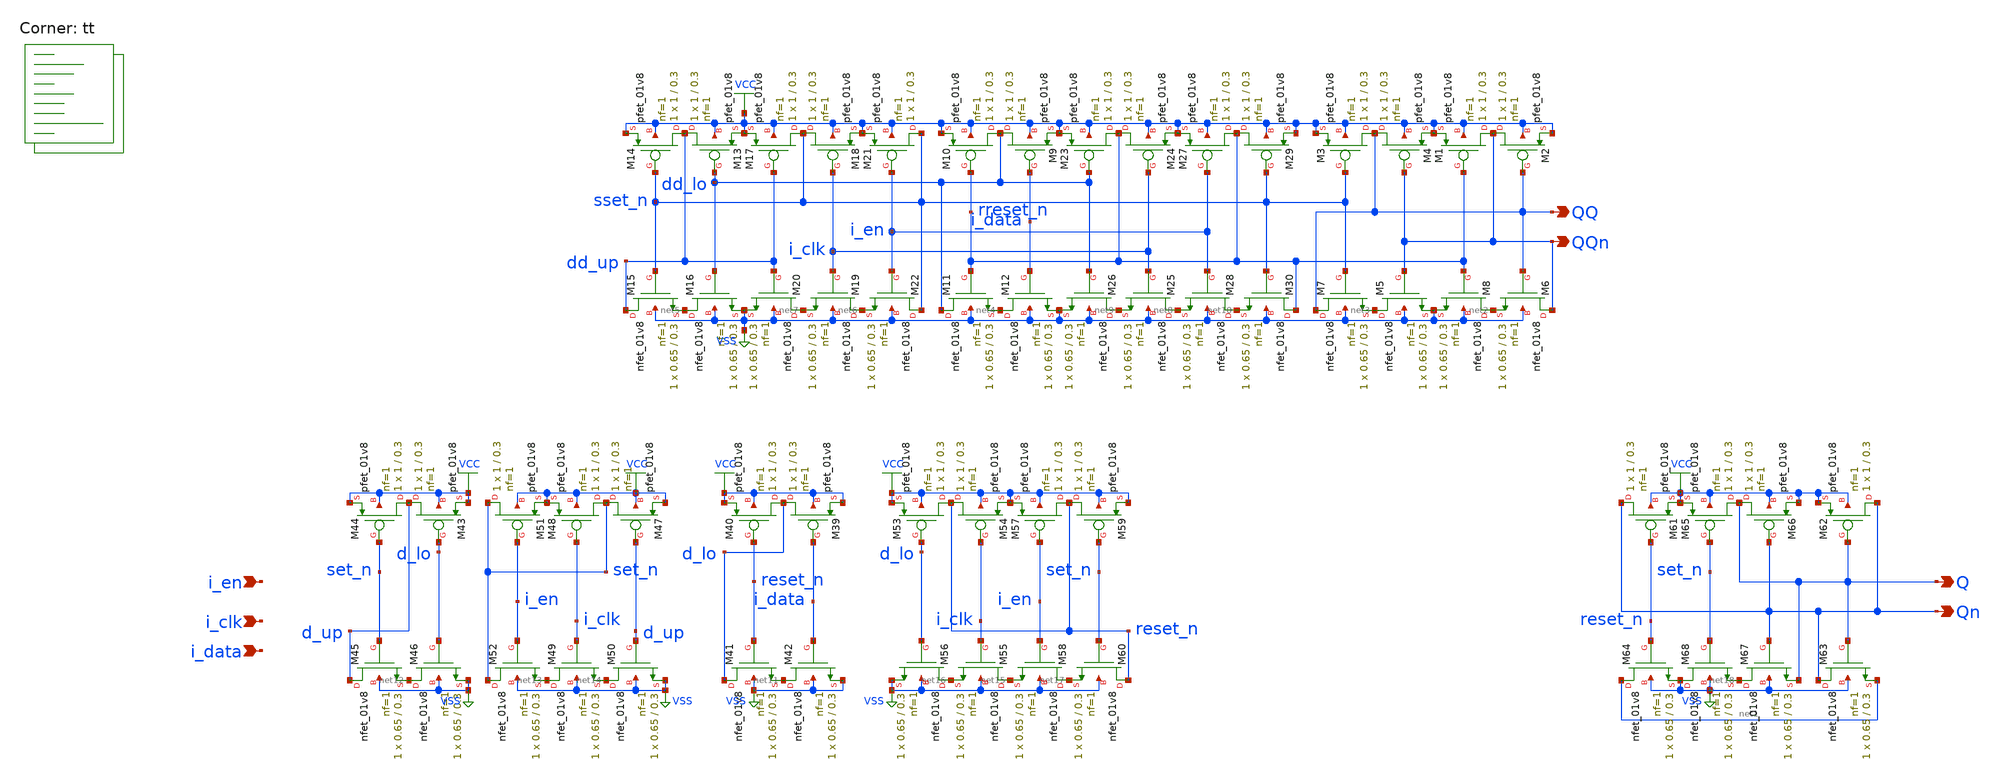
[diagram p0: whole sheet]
** sch_path: elements/edffe.sch
**.subckt edffe QQ QQn i_clk i_data i_en Q Qn
*.opin QQ
*.opin QQn
*.ipin i_clk
*.ipin i_data
*.ipin i_en
*.opin Q
*.opin Qn
XM1 QQn rreset_n VCC VCC sky130_fd_pr__pfet_01v8 L=0.3 W=1 nf=1 ad='int((nf+1)/2) * W/nf * 0.29' as='int((nf+2)/2) * W/nf * 0.29'
+ pd='2*int((nf+1)/2) * (W/nf + 0.29)' ps='2*int((nf+2)/2) * (W/nf + 0.29)' nrd='0.29 / W' nrs='0.29 / W'
+ sa=0 sb=0 sd=0 mult=1 m=1
XM2 QQn QQ VCC VCC sky130_fd_pr__pfet_01v8 L=0.3 W=1 nf=1 ad='int((nf+1)/2) * W/nf * 0.29' as='int((nf+2)/2) * W/nf * 0.29'
+ pd='2*int((nf+1)/2) * (W/nf + 0.29)' ps='2*int((nf+2)/2) * (W/nf + 0.29)' nrd='0.29 / W' nrs='0.29 / W'
+ sa=0 sb=0 sd=0 mult=1 m=1
XM6 QQn QQ net2 VSS sky130_fd_pr__nfet_01v8 L=0.3 W=0.65 nf=1 ad='int((1 + 1)/2) * 0.65 / 1 * 0.29' as='int((1 + 2)/2) * 0.65 / 1 * 0.29'
+ pd='2*int((1 + 1)/2) * (0.65 / 1 + 0.29)' ps='2*int((1 + 2)/2) * (0.65 / 1 + 0.29)' nrd='0.29 / 0.65 '
+ nrs='0.29 / 0.65 ' sa=0 sb=0 sd=0 mult=1 m=1
XM8 net2 rreset_n VSS VSS sky130_fd_pr__nfet_01v8 L=0.3 W=0.65 nf=1 ad='int((1 + 1)/2) * 0.65 / 1 * 0.29'
+ as='int((1 + 2)/2) * 0.65 / 1 * 0.29' pd='2*int((1 + 1)/2) * (0.65 / 1 + 0.29)' ps='2*int((1 + 2)/2) * (0.65 / 1 + 0.29)'
+ nrd='0.29 / 0.65 ' nrs='0.29 / 0.65 ' sa=0 sb=0 sd=0 mult=1 m=1
XM3 QQ sset_n VCC VCC sky130_fd_pr__pfet_01v8 L=0.3 W=1 nf=1 ad='int((nf+1)/2) * W/nf * 0.29' as='int((nf+2)/2) * W/nf * 0.29'
+ pd='2*int((nf+1)/2) * (W/nf + 0.29)' ps='2*int((nf+2)/2) * (W/nf + 0.29)' nrd='0.29 / W' nrs='0.29 / W'
+ sa=0 sb=0 sd=0 mult=1 m=1
XM4 QQ QQn VCC VCC sky130_fd_pr__pfet_01v8 L=0.3 W=1 nf=1 ad='int((nf+1)/2) * W/nf * 0.29' as='int((nf+2)/2) * W/nf * 0.29'
+ pd='2*int((nf+1)/2) * (W/nf + 0.29)' ps='2*int((nf+2)/2) * (W/nf + 0.29)' nrd='0.29 / W' nrs='0.29 / W'
+ sa=0 sb=0 sd=0 mult=1 m=1
XM5 net3 QQn VSS VSS sky130_fd_pr__nfet_01v8 L=0.3 W=0.65 nf=1 ad='int((1 + 1)/2) * 0.65 / 1 * 0.29'
+ as='int((1 + 2)/2) * 0.65 / 1 * 0.29' pd='2*int((1 + 1)/2) * (0.65 / 1 + 0.29)' ps='2*int((1 + 2)/2) * (0.65 / 1 + 0.29)'
+ nrd='0.29 / 0.65 ' nrs='0.29 / 0.65 ' sa=0 sb=0 sd=0 mult=1 m=1
XM7 QQ sset_n net3 VSS sky130_fd_pr__nfet_01v8 L=0.3 W=0.65 nf=1 ad='int((1 + 1)/2) * 0.65 / 1 * 0.29'
+ as='int((1 + 2)/2) * 0.65 / 1 * 0.29' pd='2*int((1 + 1)/2) * (0.65 / 1 + 0.29)' ps='2*int((1 + 2)/2) * (0.65 / 1 + 0.29)'
+ nrd='0.29 / 0.65 ' nrs='0.29 / 0.65 ' sa=0 sb=0 sd=0 mult=1 m=1
XM9 dd_lo i_data VCC VCC sky130_fd_pr__pfet_01v8 L=0.3 W=1 nf=1 ad='int((nf+1)/2) * W/nf * 0.29' as='int((nf+2)/2) * W/nf * 0.29'
+ pd='2*int((nf+1)/2) * (W/nf + 0.29)' ps='2*int((nf+2)/2) * (W/nf + 0.29)' nrd='0.29 / W' nrs='0.29 / W'
+ sa=0 sb=0 sd=0 mult=1 m=1
XM10 dd_lo rreset_n VCC VCC sky130_fd_pr__pfet_01v8 L=0.3 W=1 nf=1 ad='int((nf+1)/2) * W/nf * 0.29' as='int((nf+2)/2) * W/nf * 0.29'
+ pd='2*int((nf+1)/2) * (W/nf + 0.29)' ps='2*int((nf+2)/2) * (W/nf + 0.29)' nrd='0.29 / W' nrs='0.29 / W'
+ sa=0 sb=0 sd=0 mult=1 m=1
XM11 dd_lo rreset_n net4 VSS sky130_fd_pr__nfet_01v8 L=0.3 W=0.65 nf=1 ad='int((1 + 1)/2) * 0.65 / 1 * 0.29'
+ as='int((1 + 2)/2) * 0.65 / 1 * 0.29' pd='2*int((1 + 1)/2) * (0.65 / 1 + 0.29)' ps='2*int((1 + 2)/2) * (0.65 / 1 + 0.29)'
+ nrd='0.29 / 0.65 ' nrs='0.29 / 0.65 ' sa=0 sb=0 sd=0 mult=1 m=1
XM12 net4 i_data VSS VSS sky130_fd_pr__nfet_01v8 L=0.3 W=0.65 nf=1 ad='int((1 + 1)/2) * 0.65 / 1 * 0.29'
+ as='int((1 + 2)/2) * 0.65 / 1 * 0.29' pd='2*int((1 + 1)/2) * (0.65 / 1 + 0.29)' ps='2*int((1 + 2)/2) * (0.65 / 1 + 0.29)'
+ nrd='0.29 / 0.65 ' nrs='0.29 / 0.65 ' sa=0 sb=0 sd=0 mult=1 m=1
XM13 dd_up dd_lo VCC VCC sky130_fd_pr__pfet_01v8 L=0.3 W=1 nf=1 ad='int((nf+1)/2) * W/nf * 0.29' as='int((nf+2)/2) * W/nf * 0.29'
+ pd='2*int((nf+1)/2) * (W/nf + 0.29)' ps='2*int((nf+2)/2) * (W/nf + 0.29)' nrd='0.29 / W' nrs='0.29 / W'
+ sa=0 sb=0 sd=0 mult=1 m=1
XM14 dd_up sset_n VCC VCC sky130_fd_pr__pfet_01v8 L=0.3 W=1 nf=1 ad='int((nf+1)/2) * W/nf * 0.29' as='int((nf+2)/2) * W/nf * 0.29'
+ pd='2*int((nf+1)/2) * (W/nf + 0.29)' ps='2*int((nf+2)/2) * (W/nf + 0.29)' nrd='0.29 / W' nrs='0.29 / W'
+ sa=0 sb=0 sd=0 mult=1 m=1
XM15 dd_up sset_n net5 VSS sky130_fd_pr__nfet_01v8 L=0.3 W=0.65 nf=1 ad='int((1 + 1)/2) * 0.65 / 1 * 0.29'
+ as='int((1 + 2)/2) * 0.65 / 1 * 0.29' pd='2*int((1 + 1)/2) * (0.65 / 1 + 0.29)' ps='2*int((1 + 2)/2) * (0.65 / 1 + 0.29)'
+ nrd='0.29 / 0.65 ' nrs='0.29 / 0.65 ' sa=0 sb=0 sd=0 mult=1 m=1
XM16 net5 dd_lo VSS VSS sky130_fd_pr__nfet_01v8 L=0.3 W=0.65 nf=1 ad='int((1 + 1)/2) * 0.65 / 1 * 0.29'
+ as='int((1 + 2)/2) * 0.65 / 1 * 0.29' pd='2*int((1 + 1)/2) * (0.65 / 1 + 0.29)' ps='2*int((1 + 2)/2) * (0.65 / 1 + 0.29)'
+ nrd='0.29 / 0.65 ' nrs='0.29 / 0.65 ' sa=0 sb=0 sd=0 mult=1 m=1
XM17 sset_n dd_up VCC VCC sky130_fd_pr__pfet_01v8 L=0.3 W=1 nf=1 ad='int((nf+1)/2) * W/nf * 0.29' as='int((nf+2)/2) * W/nf * 0.29'
+ pd='2*int((nf+1)/2) * (W/nf + 0.29)' ps='2*int((nf+2)/2) * (W/nf + 0.29)' nrd='0.29 / W' nrs='0.29 / W'
+ sa=0 sb=0 sd=0 mult=1 m=1
XM18 sset_n i_clk VCC VCC sky130_fd_pr__pfet_01v8 L=0.3 W=1 nf=1 ad='int((nf+1)/2) * W/nf * 0.29' as='int((nf+2)/2) * W/nf * 0.29'
+ pd='2*int((nf+1)/2) * (W/nf + 0.29)' ps='2*int((nf+2)/2) * (W/nf + 0.29)' nrd='0.29 / W' nrs='0.29 / W'
+ sa=0 sb=0 sd=0 mult=1 m=1
XM19 net6 i_clk net7 VSS sky130_fd_pr__nfet_01v8 L=0.3 W=0.65 nf=1 ad='int((1 + 1)/2) * 0.65 / 1 * 0.29'
+ as='int((1 + 2)/2) * 0.65 / 1 * 0.29' pd='2*int((1 + 1)/2) * (0.65 / 1 + 0.29)' ps='2*int((1 + 2)/2) * (0.65 / 1 + 0.29)'
+ nrd='0.29 / 0.65 ' nrs='0.29 / 0.65 ' sa=0 sb=0 sd=0 mult=1 m=1
XM20 net7 dd_up VSS VSS sky130_fd_pr__nfet_01v8 L=0.3 W=0.65 nf=1 ad='int((1 + 1)/2) * 0.65 / 1 * 0.29'
+ as='int((1 + 2)/2) * 0.65 / 1 * 0.29' pd='2*int((1 + 1)/2) * (0.65 / 1 + 0.29)' ps='2*int((1 + 2)/2) * (0.65 / 1 + 0.29)'
+ nrd='0.29 / 0.65 ' nrs='0.29 / 0.65 ' sa=0 sb=0 sd=0 mult=1 m=1
XM21 sset_n i_en VCC VCC sky130_fd_pr__pfet_01v8 L=0.3 W=1 nf=1 ad='int((nf+1)/2) * W/nf * 0.29' as='int((nf+2)/2) * W/nf * 0.29'
+ pd='2*int((nf+1)/2) * (W/nf + 0.29)' ps='2*int((nf+2)/2) * (W/nf + 0.29)' nrd='0.29 / W' nrs='0.29 / W'
+ sa=0 sb=0 sd=0 mult=1 m=1
XM22 sset_n i_en net6 VSS sky130_fd_pr__nfet_01v8 L=0.3 W=0.65 nf=1 ad='int((1 + 1)/2) * 0.65 / 1 * 0.29'
+ as='int((1 + 2)/2) * 0.65 / 1 * 0.29' pd='2*int((1 + 1)/2) * (0.65 / 1 + 0.29)' ps='2*int((1 + 2)/2) * (0.65 / 1 + 0.29)'
+ nrd='0.29 / 0.65 ' nrs='0.29 / 0.65 ' sa=0 sb=0 sd=0 mult=1 m=1
XM23 rreset_n dd_lo VCC VCC sky130_fd_pr__pfet_01v8 L=0.3 W=1 nf=1 ad='int((nf+1)/2) * W/nf * 0.29' as='int((nf+2)/2) * W/nf * 0.29'
+ pd='2*int((nf+1)/2) * (W/nf + 0.29)' ps='2*int((nf+2)/2) * (W/nf + 0.29)' nrd='0.29 / W' nrs='0.29 / W'
+ sa=0 sb=0 sd=0 mult=1 m=1
XM24 rreset_n i_clk VCC VCC sky130_fd_pr__pfet_01v8 L=0.3 W=1 nf=1 ad='int((nf+1)/2) * W/nf * 0.29' as='int((nf+2)/2) * W/nf * 0.29'
+ pd='2*int((nf+1)/2) * (W/nf + 0.29)' ps='2*int((nf+2)/2) * (W/nf + 0.29)' nrd='0.29 / W' nrs='0.29 / W'
+ sa=0 sb=0 sd=0 mult=1 m=1
XM25 net8 i_clk net9 VSS sky130_fd_pr__nfet_01v8 L=0.3 W=0.65 nf=1 ad='int((1 + 1)/2) * 0.65 / 1 * 0.29'
+ as='int((1 + 2)/2) * 0.65 / 1 * 0.29' pd='2*int((1 + 1)/2) * (0.65 / 1 + 0.29)' ps='2*int((1 + 2)/2) * (0.65 / 1 + 0.29)'
+ nrd='0.29 / 0.65 ' nrs='0.29 / 0.65 ' sa=0 sb=0 sd=0 mult=1 m=1
XM26 net9 dd_lo VSS VSS sky130_fd_pr__nfet_01v8 L=0.3 W=0.65 nf=1 ad='int((1 + 1)/2) * 0.65 / 1 * 0.29'
+ as='int((1 + 2)/2) * 0.65 / 1 * 0.29' pd='2*int((1 + 1)/2) * (0.65 / 1 + 0.29)' ps='2*int((1 + 2)/2) * (0.65 / 1 + 0.29)'
+ nrd='0.29 / 0.65 ' nrs='0.29 / 0.65 ' sa=0 sb=0 sd=0 mult=1 m=1
XM27 rreset_n i_en VCC VCC sky130_fd_pr__pfet_01v8 L=0.3 W=1 nf=1 ad='int((nf+1)/2) * W/nf * 0.29' as='int((nf+2)/2) * W/nf * 0.29'
+ pd='2*int((nf+1)/2) * (W/nf + 0.29)' ps='2*int((nf+2)/2) * (W/nf + 0.29)' nrd='0.29 / W' nrs='0.29 / W'
+ sa=0 sb=0 sd=0 mult=1 m=1
XM28 net10 i_en net8 VSS sky130_fd_pr__nfet_01v8 L=0.3 W=0.65 nf=1 ad='int((1 + 1)/2) * 0.65 / 1 * 0.29'
+ as='int((1 + 2)/2) * 0.65 / 1 * 0.29' pd='2*int((1 + 1)/2) * (0.65 / 1 + 0.29)' ps='2*int((1 + 2)/2) * (0.65 / 1 + 0.29)'
+ nrd='0.29 / 0.65 ' nrs='0.29 / 0.65 ' sa=0 sb=0 sd=0 mult=1 m=1
XM29 rreset_n sset_n VCC VCC sky130_fd_pr__pfet_01v8 L=0.3 W=1 nf=1 ad='int((nf+1)/2) * W/nf * 0.29'
+ as='int((nf+2)/2) * W/nf * 0.29' pd='2*int((nf+1)/2) * (W/nf + 0.29)' ps='2*int((nf+2)/2) * (W/nf + 0.29)'
+ nrd='0.29 / W' nrs='0.29 / W' sa=0 sb=0 sd=0 mult=1 m=1
XM30 rreset_n sset_n net10 VSS sky130_fd_pr__nfet_01v8 L=0.3 W=0.65 nf=1 ad='int((1 + 1)/2) * 0.65 / 1 * 0.29'
+ as='int((1 + 2)/2) * 0.65 / 1 * 0.29' pd='2*int((1 + 1)/2) * (0.65 / 1 + 0.29)' ps='2*int((1 + 2)/2) * (0.65 / 1 + 0.29)'
+ nrd='0.29 / 0.65 ' nrs='0.29 / 0.65 ' sa=0 sb=0 sd=0 mult=1 m=1
XM39 d_lo i_data VCC VCC sky130_fd_pr__pfet_01v8 L=0.3 W=1 nf=1 ad='int((nf+1)/2) * W/nf * 0.29' as='int((nf+2)/2) * W/nf * 0.29'
+ pd='2*int((nf+1)/2) * (W/nf + 0.29)' ps='2*int((nf+2)/2) * (W/nf + 0.29)' nrd='0.29 / W' nrs='0.29 / W'
+ sa=0 sb=0 sd=0 mult=1 m=1
XM40 d_lo reset_n VCC VCC sky130_fd_pr__pfet_01v8 L=0.3 W=1 nf=1 ad='int((nf+1)/2) * W/nf * 0.29' as='int((nf+2)/2) * W/nf * 0.29'
+ pd='2*int((nf+1)/2) * (W/nf + 0.29)' ps='2*int((nf+2)/2) * (W/nf + 0.29)' nrd='0.29 / W' nrs='0.29 / W'
+ sa=0 sb=0 sd=0 mult=1 m=1
XM41 d_lo reset_n net11 VSS sky130_fd_pr__nfet_01v8 L=0.3 W=0.65 nf=1 ad='int((1 + 1)/2) * 0.65 / 1 * 0.29'
+ as='int((1 + 2)/2) * 0.65 / 1 * 0.29' pd='2*int((1 + 1)/2) * (0.65 / 1 + 0.29)' ps='2*int((1 + 2)/2) * (0.65 / 1 + 0.29)'
+ nrd='0.29 / 0.65 ' nrs='0.29 / 0.65 ' sa=0 sb=0 sd=0 mult=1 m=1
XM42 net11 i_data VSS VSS sky130_fd_pr__nfet_01v8 L=0.3 W=0.65 nf=1 ad='int((1 + 1)/2) * 0.65 / 1 * 0.29'
+ as='int((1 + 2)/2) * 0.65 / 1 * 0.29' pd='2*int((1 + 1)/2) * (0.65 / 1 + 0.29)' ps='2*int((1 + 2)/2) * (0.65 / 1 + 0.29)'
+ nrd='0.29 / 0.65 ' nrs='0.29 / 0.65 ' sa=0 sb=0 sd=0 mult=1 m=1
XM43 d_up d_lo VCC VCC sky130_fd_pr__pfet_01v8 L=0.3 W=1 nf=1 ad='int((nf+1)/2) * W/nf * 0.29' as='int((nf+2)/2) * W/nf * 0.29'
+ pd='2*int((nf+1)/2) * (W/nf + 0.29)' ps='2*int((nf+2)/2) * (W/nf + 0.29)' nrd='0.29 / W' nrs='0.29 / W'
+ sa=0 sb=0 sd=0 mult=1 m=1
XM44 d_up set_n VCC VCC sky130_fd_pr__pfet_01v8 L=0.3 W=1 nf=1 ad='int((nf+1)/2) * W/nf * 0.29' as='int((nf+2)/2) * W/nf * 0.29'
+ pd='2*int((nf+1)/2) * (W/nf + 0.29)' ps='2*int((nf+2)/2) * (W/nf + 0.29)' nrd='0.29 / W' nrs='0.29 / W'
+ sa=0 sb=0 sd=0 mult=1 m=1
XM45 d_up set_n net12 VSS sky130_fd_pr__nfet_01v8 L=0.3 W=0.65 nf=1 ad='int((1 + 1)/2) * 0.65 / 1 * 0.29'
+ as='int((1 + 2)/2) * 0.65 / 1 * 0.29' pd='2*int((1 + 1)/2) * (0.65 / 1 + 0.29)' ps='2*int((1 + 2)/2) * (0.65 / 1 + 0.29)'
+ nrd='0.29 / 0.65 ' nrs='0.29 / 0.65 ' sa=0 sb=0 sd=0 mult=1 m=1
XM46 net12 d_lo VSS VSS sky130_fd_pr__nfet_01v8 L=0.3 W=0.65 nf=1 ad='int((1 + 1)/2) * 0.65 / 1 * 0.29'
+ as='int((1 + 2)/2) * 0.65 / 1 * 0.29' pd='2*int((1 + 1)/2) * (0.65 / 1 + 0.29)' ps='2*int((1 + 2)/2) * (0.65 / 1 + 0.29)'
+ nrd='0.29 / 0.65 ' nrs='0.29 / 0.65 ' sa=0 sb=0 sd=0 mult=1 m=1
XM47 set_n d_up VCC VCC sky130_fd_pr__pfet_01v8 L=0.3 W=1 nf=1 ad='int((nf+1)/2) * W/nf * 0.29' as='int((nf+2)/2) * W/nf * 0.29'
+ pd='2*int((nf+1)/2) * (W/nf + 0.29)' ps='2*int((nf+2)/2) * (W/nf + 0.29)' nrd='0.29 / W' nrs='0.29 / W'
+ sa=0 sb=0 sd=0 mult=1 m=1
XM48 set_n i_clk VCC VCC sky130_fd_pr__pfet_01v8 L=0.3 W=1 nf=1 ad='int((nf+1)/2) * W/nf * 0.29' as='int((nf+2)/2) * W/nf * 0.29'
+ pd='2*int((nf+1)/2) * (W/nf + 0.29)' ps='2*int((nf+2)/2) * (W/nf + 0.29)' nrd='0.29 / W' nrs='0.29 / W'
+ sa=0 sb=0 sd=0 mult=1 m=1
XM49 net13 i_clk net14 VSS sky130_fd_pr__nfet_01v8 L=0.3 W=0.65 nf=1 ad='int((1 + 1)/2) * 0.65 / 1 * 0.29'
+ as='int((1 + 2)/2) * 0.65 / 1 * 0.29' pd='2*int((1 + 1)/2) * (0.65 / 1 + 0.29)' ps='2*int((1 + 2)/2) * (0.65 / 1 + 0.29)'
+ nrd='0.29 / 0.65 ' nrs='0.29 / 0.65 ' sa=0 sb=0 sd=0 mult=1 m=1
XM50 net14 d_up VSS VSS sky130_fd_pr__nfet_01v8 L=0.3 W=0.65 nf=1 ad='int((1 + 1)/2) * 0.65 / 1 * 0.29'
+ as='int((1 + 2)/2) * 0.65 / 1 * 0.29' pd='2*int((1 + 1)/2) * (0.65 / 1 + 0.29)' ps='2*int((1 + 2)/2) * (0.65 / 1 + 0.29)'
+ nrd='0.29 / 0.65 ' nrs='0.29 / 0.65 ' sa=0 sb=0 sd=0 mult=1 m=1
XM51 set_n i_en VCC VCC sky130_fd_pr__pfet_01v8 L=0.3 W=1 nf=1 ad='int((nf+1)/2) * W/nf * 0.29' as='int((nf+2)/2) * W/nf * 0.29'
+ pd='2*int((nf+1)/2) * (W/nf + 0.29)' ps='2*int((nf+2)/2) * (W/nf + 0.29)' nrd='0.29 / W' nrs='0.29 / W'
+ sa=0 sb=0 sd=0 mult=1 m=1
XM52 set_n i_en net13 VSS sky130_fd_pr__nfet_01v8 L=0.3 W=0.65 nf=1 ad='int((1 + 1)/2) * 0.65 / 1 * 0.29'
+ as='int((1 + 2)/2) * 0.65 / 1 * 0.29' pd='2*int((1 + 1)/2) * (0.65 / 1 + 0.29)' ps='2*int((1 + 2)/2) * (0.65 / 1 + 0.29)'
+ nrd='0.29 / 0.65 ' nrs='0.29 / 0.65 ' sa=0 sb=0 sd=0 mult=1 m=1
XM53 reset_n d_lo VCC VCC sky130_fd_pr__pfet_01v8 L=0.3 W=1 nf=1 ad='int((nf+1)/2) * W/nf * 0.29' as='int((nf+2)/2) * W/nf * 0.29'
+ pd='2*int((nf+1)/2) * (W/nf + 0.29)' ps='2*int((nf+2)/2) * (W/nf + 0.29)' nrd='0.29 / W' nrs='0.29 / W'
+ sa=0 sb=0 sd=0 mult=1 m=1
XM54 reset_n i_clk VCC VCC sky130_fd_pr__pfet_01v8 L=0.3 W=1 nf=1 ad='int((nf+1)/2) * W/nf * 0.29' as='int((nf+2)/2) * W/nf * 0.29'
+ pd='2*int((nf+1)/2) * (W/nf + 0.29)' ps='2*int((nf+2)/2) * (W/nf + 0.29)' nrd='0.29 / W' nrs='0.29 / W'
+ sa=0 sb=0 sd=0 mult=1 m=1
XM55 net15 i_clk net16 VSS sky130_fd_pr__nfet_01v8 L=0.3 W=0.65 nf=1 ad='int((1 + 1)/2) * 0.65 / 1 * 0.29'
+ as='int((1 + 2)/2) * 0.65 / 1 * 0.29' pd='2*int((1 + 1)/2) * (0.65 / 1 + 0.29)' ps='2*int((1 + 2)/2) * (0.65 / 1 + 0.29)'
+ nrd='0.29 / 0.65 ' nrs='0.29 / 0.65 ' sa=0 sb=0 sd=0 mult=1 m=1
XM56 net16 d_lo VSS VSS sky130_fd_pr__nfet_01v8 L=0.3 W=0.65 nf=1 ad='int((1 + 1)/2) * 0.65 / 1 * 0.29'
+ as='int((1 + 2)/2) * 0.65 / 1 * 0.29' pd='2*int((1 + 1)/2) * (0.65 / 1 + 0.29)' ps='2*int((1 + 2)/2) * (0.65 / 1 + 0.29)'
+ nrd='0.29 / 0.65 ' nrs='0.29 / 0.65 ' sa=0 sb=0 sd=0 mult=1 m=1
XM57 reset_n i_en VCC VCC sky130_fd_pr__pfet_01v8 L=0.3 W=1 nf=1 ad='int((nf+1)/2) * W/nf * 0.29' as='int((nf+2)/2) * W/nf * 0.29'
+ pd='2*int((nf+1)/2) * (W/nf + 0.29)' ps='2*int((nf+2)/2) * (W/nf + 0.29)' nrd='0.29 / W' nrs='0.29 / W'
+ sa=0 sb=0 sd=0 mult=1 m=1
XM58 net17 i_en net15 VSS sky130_fd_pr__nfet_01v8 L=0.3 W=0.65 nf=1 ad='int((1 + 1)/2) * 0.65 / 1 * 0.29'
+ as='int((1 + 2)/2) * 0.65 / 1 * 0.29' pd='2*int((1 + 1)/2) * (0.65 / 1 + 0.29)' ps='2*int((1 + 2)/2) * (0.65 / 1 + 0.29)'
+ nrd='0.29 / 0.65 ' nrs='0.29 / 0.65 ' sa=0 sb=0 sd=0 mult=1 m=1
XM59 reset_n set_n VCC VCC sky130_fd_pr__pfet_01v8 L=0.3 W=1 nf=1 ad='int((nf+1)/2) * W/nf * 0.29' as='int((nf+2)/2) * W/nf * 0.29'
+ pd='2*int((nf+1)/2) * (W/nf + 0.29)' ps='2*int((nf+2)/2) * (W/nf + 0.29)' nrd='0.29 / W' nrs='0.29 / W'
+ sa=0 sb=0 sd=0 mult=1 m=1
XM60 reset_n set_n net17 VSS sky130_fd_pr__nfet_01v8 L=0.3 W=0.65 nf=1 ad='int((1 + 1)/2) * 0.65 / 1 * 0.29'
+ as='int((1 + 2)/2) * 0.65 / 1 * 0.29' pd='2*int((1 + 1)/2) * (0.65 / 1 + 0.29)' ps='2*int((1 + 2)/2) * (0.65 / 1 + 0.29)'
+ nrd='0.29 / 0.65 ' nrs='0.29 / 0.65 ' sa=0 sb=0 sd=0 mult=1 m=1
XM61 Qn reset_n VCC VCC sky130_fd_pr__pfet_01v8 L=0.3 W=1 nf=1 ad='int((nf+1)/2) * W/nf * 0.29' as='int((nf+2)/2) * W/nf * 0.29'
+ pd='2*int((nf+1)/2) * (W/nf + 0.29)' ps='2*int((nf+2)/2) * (W/nf + 0.29)' nrd='0.29 / W' nrs='0.29 / W'
+ sa=0 sb=0 sd=0 mult=1 m=1
XM62 Qn Q VCC VCC sky130_fd_pr__pfet_01v8 L=0.3 W=1 nf=1 ad='int((nf+1)/2) * W/nf * 0.29' as='int((nf+2)/2) * W/nf * 0.29'
+ pd='2*int((nf+1)/2) * (W/nf + 0.29)' ps='2*int((nf+2)/2) * (W/nf + 0.29)' nrd='0.29 / W' nrs='0.29 / W'
+ sa=0 sb=0 sd=0 mult=1 m=1
XM63 Qn Q net1 VSS sky130_fd_pr__nfet_01v8 L=0.3 W=0.65 nf=1 ad='int((1 + 1)/2) * 0.65 / 1 * 0.29' as='int((1 + 2)/2) * 0.65 / 1 * 0.29'
+ pd='2*int((1 + 1)/2) * (0.65 / 1 + 0.29)' ps='2*int((1 + 2)/2) * (0.65 / 1 + 0.29)' nrd='0.29 / 0.65 '
+ nrs='0.29 / 0.65 ' sa=0 sb=0 sd=0 mult=1 m=1
XM64 net1 reset_n VSS VSS sky130_fd_pr__nfet_01v8 L=0.3 W=0.65 nf=1 ad='int((1 + 1)/2) * 0.65 / 1 * 0.29'
+ as='int((1 + 2)/2) * 0.65 / 1 * 0.29' pd='2*int((1 + 1)/2) * (0.65 / 1 + 0.29)' ps='2*int((1 + 2)/2) * (0.65 / 1 + 0.29)'
+ nrd='0.29 / 0.65 ' nrs='0.29 / 0.65 ' sa=0 sb=0 sd=0 mult=1 m=1
XM65 Q set_n VCC VCC sky130_fd_pr__pfet_01v8 L=0.3 W=1 nf=1 ad='int((nf+1)/2) * W/nf * 0.29' as='int((nf+2)/2) * W/nf * 0.29'
+ pd='2*int((nf+1)/2) * (W/nf + 0.29)' ps='2*int((nf+2)/2) * (W/nf + 0.29)' nrd='0.29 / W' nrs='0.29 / W'
+ sa=0 sb=0 sd=0 mult=1 m=1
XM66 Q Qn VCC VCC sky130_fd_pr__pfet_01v8 L=0.3 W=1 nf=1 ad='int((nf+1)/2) * W/nf * 0.29' as='int((nf+2)/2) * W/nf * 0.29'
+ pd='2*int((nf+1)/2) * (W/nf + 0.29)' ps='2*int((nf+2)/2) * (W/nf + 0.29)' nrd='0.29 / W' nrs='0.29 / W'
+ sa=0 sb=0 sd=0 mult=1 m=1
XM67 net18 Qn Q VSS sky130_fd_pr__nfet_01v8 L=0.3 W=0.65 nf=1 ad='int((1 + 1)/2) * 0.65 / 1 * 0.29' as='int((1 + 2)/2) * 0.65 / 1 * 0.29'
+ pd='2*int((1 + 1)/2) * (0.65 / 1 + 0.29)' ps='2*int((1 + 2)/2) * (0.65 / 1 + 0.29)' nrd='0.29 / 0.65 '
+ nrs='0.29 / 0.65 ' sa=0 sb=0 sd=0 mult=1 m=1
XM68 VSS set_n net18 VSS sky130_fd_pr__nfet_01v8 L=0.3 W=0.65 nf=1 ad='int((1 + 1)/2) * 0.65 / 1 * 0.29'
+ as='int((1 + 2)/2) * 0.65 / 1 * 0.29' pd='2*int((1 + 1)/2) * (0.65 / 1 + 0.29)' ps='2*int((1 + 2)/2) * (0.65 / 1 + 0.29)'
+ nrd='0.29 / 0.65 ' nrs='0.29 / 0.65 ' sa=0 sb=0 sd=0 mult=1 m=1
**** begin user architecture code
.lib $::SKYWATER_MODELS/sky130.lib.spice tt

.include $::SKYWATER_STDCELLS/sky130_fd_sc_hd.spice




*.option method=gear
.param VCC=1.8

.include stimuli_edffe.cir
.control
* save all
tran 0.1n 40n uic
write edffe.raw
acct
rusage
.endc






**** end user architecture code
**.ends
.GLOBAL VCC
.GLOBAL VSS
.end
